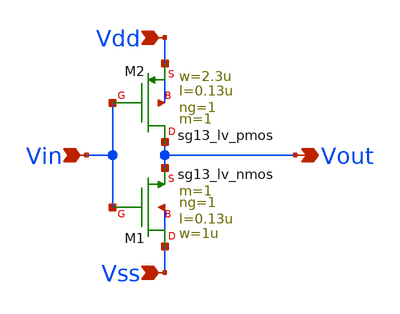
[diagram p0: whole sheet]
** sch_path: xschem/sch/inv_lv.sch
**.subckt inv_lv Vdd Vss Vin Vout
*.ipin Vdd
*.ipin Vss
*.ipin Vin
*.opin Vout
XM1 Vss Vin Vout Vss sg13_lv_nmos w=1u l=0.13u ng=1 m=1 mm_ok=1
XM2 Vout Vin Vdd Vdd sg13_lv_pmos w=2.3u l=0.13u ng=1 m=1 mm_ok=1
**.ends
.end
